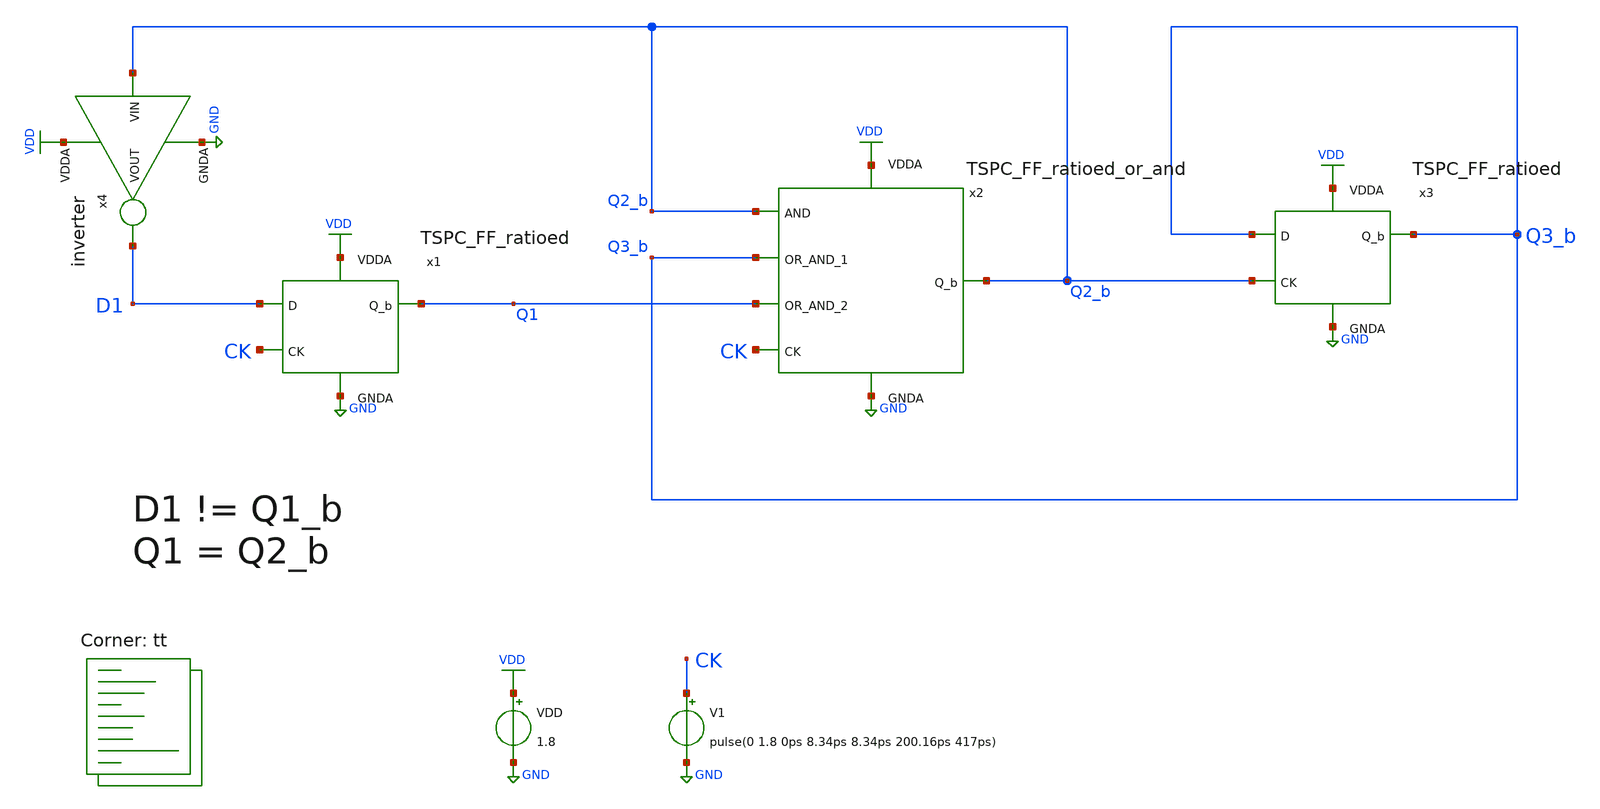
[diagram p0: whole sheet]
** sch_path: projects/pll/divider/xschem_ngspice/tb_TSPC_FF_ratioed_divide5_2.sch
**.subckt tb_TSPC_FF_ratioed_divide5_2
VDD VDD GND 1.8
V1 CK GND pulse(0 1.8 0ps 8.34ps 8.34ps 200.16ps 417ps)
x1 VDD Q1 D1 CK GND TSPC_FF_ratioed
x2 VDD Q2_b Q2_b Q3_b Q1 CK GND TSPC_FF_ratioed_or_and
x3 VDD Q3_b Q3_b Q2_b GND TSPC_FF_ratioed
x4 VDD Q2_b D1 GND inverter
**** begin user architecture code



.include /foss/pdks/sky130A/libs.ref/sky130_fd_sc_hd/spice/sky130_fd_sc_hd.spice

.option method=gear
.option wnflag=1
.option savecurrents


*.ic v(d)=0
*.ic v(q)=0
*.ic v(q1)=0

.control

  save v(d1) v(q1) v(q2_b) v(q3_b) v(ck)
  * save all
  * tran 0.1n 1u
  tran 1p 40n

  remzerovec
  write tb_TSPC_FF_ratioed_divide5_2.raw
  * set appendwrite

.endc



.lib $::SKYWATER_MODELS/sky130.lib.spice tt
**** end user architecture code
**.ends

* expanding   symbol:
*+  /foss/designs/my_design/projects/pll/divider/xschem_ngspice/TSPC_FF_ratioed.sym # of pins=5
** sym_path: projects/pll/divider/xschem_ngspice/TSPC_FF_ratioed.sym
** sch_path: projects/pll/divider/xschem_ngspice/TSPC_FF_ratioed.sch
.subckt TSPC_FF_ratioed VDDA Q_b D CK GNDA
*.ipin CK
*.ipin D
*.opin Q_b
*.ipin VDDA
*.ipin GNDA
XM1 Q_b CK VDDA VDDA sky130_fd_pr__pfet_01v8 L=0.15 W=1 nf=1 ad='int((nf+1)/2) * W/nf * 0.29' as='int((nf+2)/2) * W/nf * 0.29'
+ pd='2*int((nf+1)/2) * (W/nf + 0.29)' ps='2*int((nf+2)/2) * (W/nf + 0.29)' nrd='0.29 / W' nrs='0.29 / W'
+ sa=0 sb=0 sd=0 mult=1 m=1
XM2 Q_b net2 GNDA GNDA sky130_fd_pr__nfet_01v8 L=0.15 W=1 nf=1 ad='int((nf+1)/2) * W/nf * 0.29' as='int((nf+2)/2) * W/nf * 0.29'
+ pd='2*int((nf+1)/2) * (W/nf + 0.29)' ps='2*int((nf+2)/2) * (W/nf + 0.29)' nrd='0.29 / W' nrs='0.29 / W'
+ sa=0 sb=0 sd=0 mult=1 m=1
XM3 net2 net3 VDDA VDDA sky130_fd_pr__pfet_01v8 L=0.15 W=1 nf=1 ad='int((nf+1)/2) * W/nf * 0.29' as='int((nf+2)/2) * W/nf * 0.29'
+ pd='2*int((nf+1)/2) * (W/nf + 0.29)' ps='2*int((nf+2)/2) * (W/nf + 0.29)' nrd='0.29 / W' nrs='0.29 / W'
+ sa=0 sb=0 sd=0 mult=1 m=1
XM4 net2 CK GNDA GNDA sky130_fd_pr__nfet_01v8 L=0.15 W=3 nf=3 ad='int((nf+1)/2) * W/nf * 0.29' as='int((nf+2)/2) * W/nf * 0.29'
+ pd='2*int((nf+1)/2) * (W/nf + 0.29)' ps='2*int((nf+2)/2) * (W/nf + 0.29)' nrd='0.29 / W' nrs='0.29 / W'
+ sa=0 sb=0 sd=0 mult=1 m=1
XM5 net3 D VDDA VDDA sky130_fd_pr__pfet_01v8 L=0.15 W=1 nf=1 ad='int((nf+1)/2) * W/nf * 0.29' as='int((nf+2)/2) * W/nf * 0.29'
+ pd='2*int((nf+1)/2) * (W/nf + 0.29)' ps='2*int((nf+2)/2) * (W/nf + 0.29)' nrd='0.29 / W' nrs='0.29 / W'
+ sa=0 sb=0 sd=0 mult=1 m=1
XM7 net1 D GNDA GNDA sky130_fd_pr__nfet_01v8 L=0.15 W=1 nf=1 ad='int((nf+1)/2) * W/nf * 0.29' as='int((nf+2)/2) * W/nf * 0.29'
+ pd='2*int((nf+1)/2) * (W/nf + 0.29)' ps='2*int((nf+2)/2) * (W/nf + 0.29)' nrd='0.29 / W' nrs='0.29 / W'
+ sa=0 sb=0 sd=0 mult=1 m=1
XM6 net3 CK net1 GNDA sky130_fd_pr__nfet_01v8 L=0.15 W=1 nf=1 ad='int((nf+1)/2) * W/nf * 0.29' as='int((nf+2)/2) * W/nf * 0.29'
+ pd='2*int((nf+1)/2) * (W/nf + 0.29)' ps='2*int((nf+2)/2) * (W/nf + 0.29)' nrd='0.29 / W' nrs='0.29 / W'
+ sa=0 sb=0 sd=0 mult=1 m=1
.ends


* expanding   symbol:
*+  /foss/designs/my_design/projects/pll/divider/xschem_ngspice/TSPC_FF_ratioed_or_and.sym # of pins=7
** sym_path: projects/pll/divider/xschem_ngspice/TSPC_FF_ratioed_or_and.sym
** sch_path: projects/pll/divider/xschem_ngspice/TSPC_FF_ratioed_or_and.sch
.subckt TSPC_FF_ratioed_or_and VDDA Q_b AND OR_AND_1 OR_AND_2 CK GNDA
*.ipin CK
*.ipin OR_AND_1
*.opin Q_b
*.ipin VDDA
*.ipin GNDA
*.ipin AND
*.ipin OR_AND_2
XM1 Q_b CK VDDA VDDA sky130_fd_pr__pfet_01v8 L=0.15 W=1 nf=1 ad='int((nf+1)/2) * W/nf * 0.29' as='int((nf+2)/2) * W/nf * 0.29'
+ pd='2*int((nf+1)/2) * (W/nf + 0.29)' ps='2*int((nf+2)/2) * (W/nf + 0.29)' nrd='0.29 / W' nrs='0.29 / W'
+ sa=0 sb=0 sd=0 mult=1 m=1
XM2 Q_b B GNDA GNDA sky130_fd_pr__nfet_01v8 L=0.15 W=1 nf=1 ad='int((nf+1)/2) * W/nf * 0.29' as='int((nf+2)/2) * W/nf * 0.29'
+ pd='2*int((nf+1)/2) * (W/nf + 0.29)' ps='2*int((nf+2)/2) * (W/nf + 0.29)' nrd='0.29 / W' nrs='0.29 / W'
+ sa=0 sb=0 sd=0 mult=1 m=1
XM3 B net1 VDDA VDDA sky130_fd_pr__pfet_01v8 L=0.15 W=1 nf=1 ad='int((nf+1)/2) * W/nf * 0.29' as='int((nf+2)/2) * W/nf * 0.29'
+ pd='2*int((nf+1)/2) * (W/nf + 0.29)' ps='2*int((nf+2)/2) * (W/nf + 0.29)' nrd='0.29 / W' nrs='0.29 / W'
+ sa=0 sb=0 sd=0 mult=1 m=1
XM4 B CK GNDA GNDA sky130_fd_pr__nfet_01v8 L=0.15 W=3 nf=3 ad='int((nf+1)/2) * W/nf * 0.29' as='int((nf+2)/2) * W/nf * 0.29'
+ pd='2*int((nf+1)/2) * (W/nf + 0.29)' ps='2*int((nf+2)/2) * (W/nf + 0.29)' nrd='0.29 / W' nrs='0.29 / W'
+ sa=0 sb=0 sd=0 mult=1 m=1
XM5 net1 OR_AND_2 net4 VDDA sky130_fd_pr__pfet_01v8 L=0.15 W=1 nf=1 ad='int((nf+1)/2) * W/nf * 0.29'
+ as='int((nf+2)/2) * W/nf * 0.29' pd='2*int((nf+1)/2) * (W/nf + 0.29)' ps='2*int((nf+2)/2) * (W/nf + 0.29)'
+ nrd='0.29 / W' nrs='0.29 / W' sa=0 sb=0 sd=0 mult=1 m=1
XM9 net3 OR_AND_2 GNDA GNDA sky130_fd_pr__nfet_01v8 L=0.15 W=1 nf=1 ad='int((nf+1)/2) * W/nf * 0.29'
+ as='int((nf+2)/2) * W/nf * 0.29' pd='2*int((nf+1)/2) * (W/nf + 0.29)' ps='2*int((nf+2)/2) * (W/nf + 0.29)'
+ nrd='0.29 / W' nrs='0.29 / W' sa=0 sb=0 sd=0 mult=1 m=1
XM7 net1 CK net2 GNDA sky130_fd_pr__nfet_01v8 L=0.15 W=1 nf=1 ad='int((nf+1)/2) * W/nf * 0.29' as='int((nf+2)/2) * W/nf * 0.29'
+ pd='2*int((nf+1)/2) * (W/nf + 0.29)' ps='2*int((nf+2)/2) * (W/nf + 0.29)' nrd='0.29 / W' nrs='0.29 / W'
+ sa=0 sb=0 sd=0 mult=1 m=1
XM6 net1 AND VDDA VDDA sky130_fd_pr__pfet_01v8 L=0.15 W=1 nf=1 ad='int((nf+1)/2) * W/nf * 0.29' as='int((nf+2)/2) * W/nf * 0.29'
+ pd='2*int((nf+1)/2) * (W/nf + 0.29)' ps='2*int((nf+2)/2) * (W/nf + 0.29)' nrd='0.29 / W' nrs='0.29 / W'
+ sa=0 sb=0 sd=0 mult=1 m=1
XM8 net2 AND net3 GNDA sky130_fd_pr__nfet_01v8 L=0.15 W=1 nf=1 ad='int((nf+1)/2) * W/nf * 0.29' as='int((nf+2)/2) * W/nf * 0.29'
+ pd='2*int((nf+1)/2) * (W/nf + 0.29)' ps='2*int((nf+2)/2) * (W/nf + 0.29)' nrd='0.29 / W' nrs='0.29 / W'
+ sa=0 sb=0 sd=0 mult=1 m=1
XM10 net4 OR_AND_1 VDDA VDDA sky130_fd_pr__pfet_01v8 L=0.15 W=1 nf=1 ad='int((nf+1)/2) * W/nf * 0.29'
+ as='int((nf+2)/2) * W/nf * 0.29' pd='2*int((nf+1)/2) * (W/nf + 0.29)' ps='2*int((nf+2)/2) * (W/nf + 0.29)'
+ nrd='0.29 / W' nrs='0.29 / W' sa=0 sb=0 sd=0 mult=1 m=1
XM11 net3 OR_AND_1 GNDA GNDA sky130_fd_pr__nfet_01v8 L=0.15 W=1 nf=1 ad='int((nf+1)/2) * W/nf * 0.29'
+ as='int((nf+2)/2) * W/nf * 0.29' pd='2*int((nf+1)/2) * (W/nf + 0.29)' ps='2*int((nf+2)/2) * (W/nf + 0.29)'
+ nrd='0.29 / W' nrs='0.29 / W' sa=0 sb=0 sd=0 mult=1 m=1
.ends


* expanding   symbol:  /foss/designs/my_design/projects/pll/divider/xschem_ngspice/inverter.sym # of
*+ pins=4
** sym_path: projects/pll/divider/xschem_ngspice/inverter.sym
** sch_path: projects/pll/divider/xschem_ngspice/inverter.sch
.subckt inverter VDDA VIN VOUT GNDA
*.ipin VIN
*.ipin VDDA
*.ipin GNDA
*.opin VOUT
XM31 VOUT VIN VDDA VDDA sky130_fd_pr__pfet_01v8 L=0.15 W=2 nf=2 ad='int((nf+1)/2) * W/nf * 0.29' as='int((nf+2)/2) * W/nf * 0.29'
+ pd='2*int((nf+1)/2) * (W/nf + 0.29)' ps='2*int((nf+2)/2) * (W/nf + 0.29)' nrd='0.29 / W' nrs='0.29 / W'
+ sa=0 sb=0 sd=0 mult=1 m=1
XM32 VOUT VIN GNDA GNDA sky130_fd_pr__nfet_01v8 L=0.15 W=1 nf=1 ad='int((nf+1)/2) * W/nf * 0.29' as='int((nf+2)/2) * W/nf * 0.29'
+ pd='2*int((nf+1)/2) * (W/nf + 0.29)' ps='2*int((nf+2)/2) * (W/nf + 0.29)' nrd='0.29 / W' nrs='0.29 / W'
+ sa=0 sb=0 sd=0 mult=1 m=1
.ends

.GLOBAL GND
.GLOBAL VDD
.end
